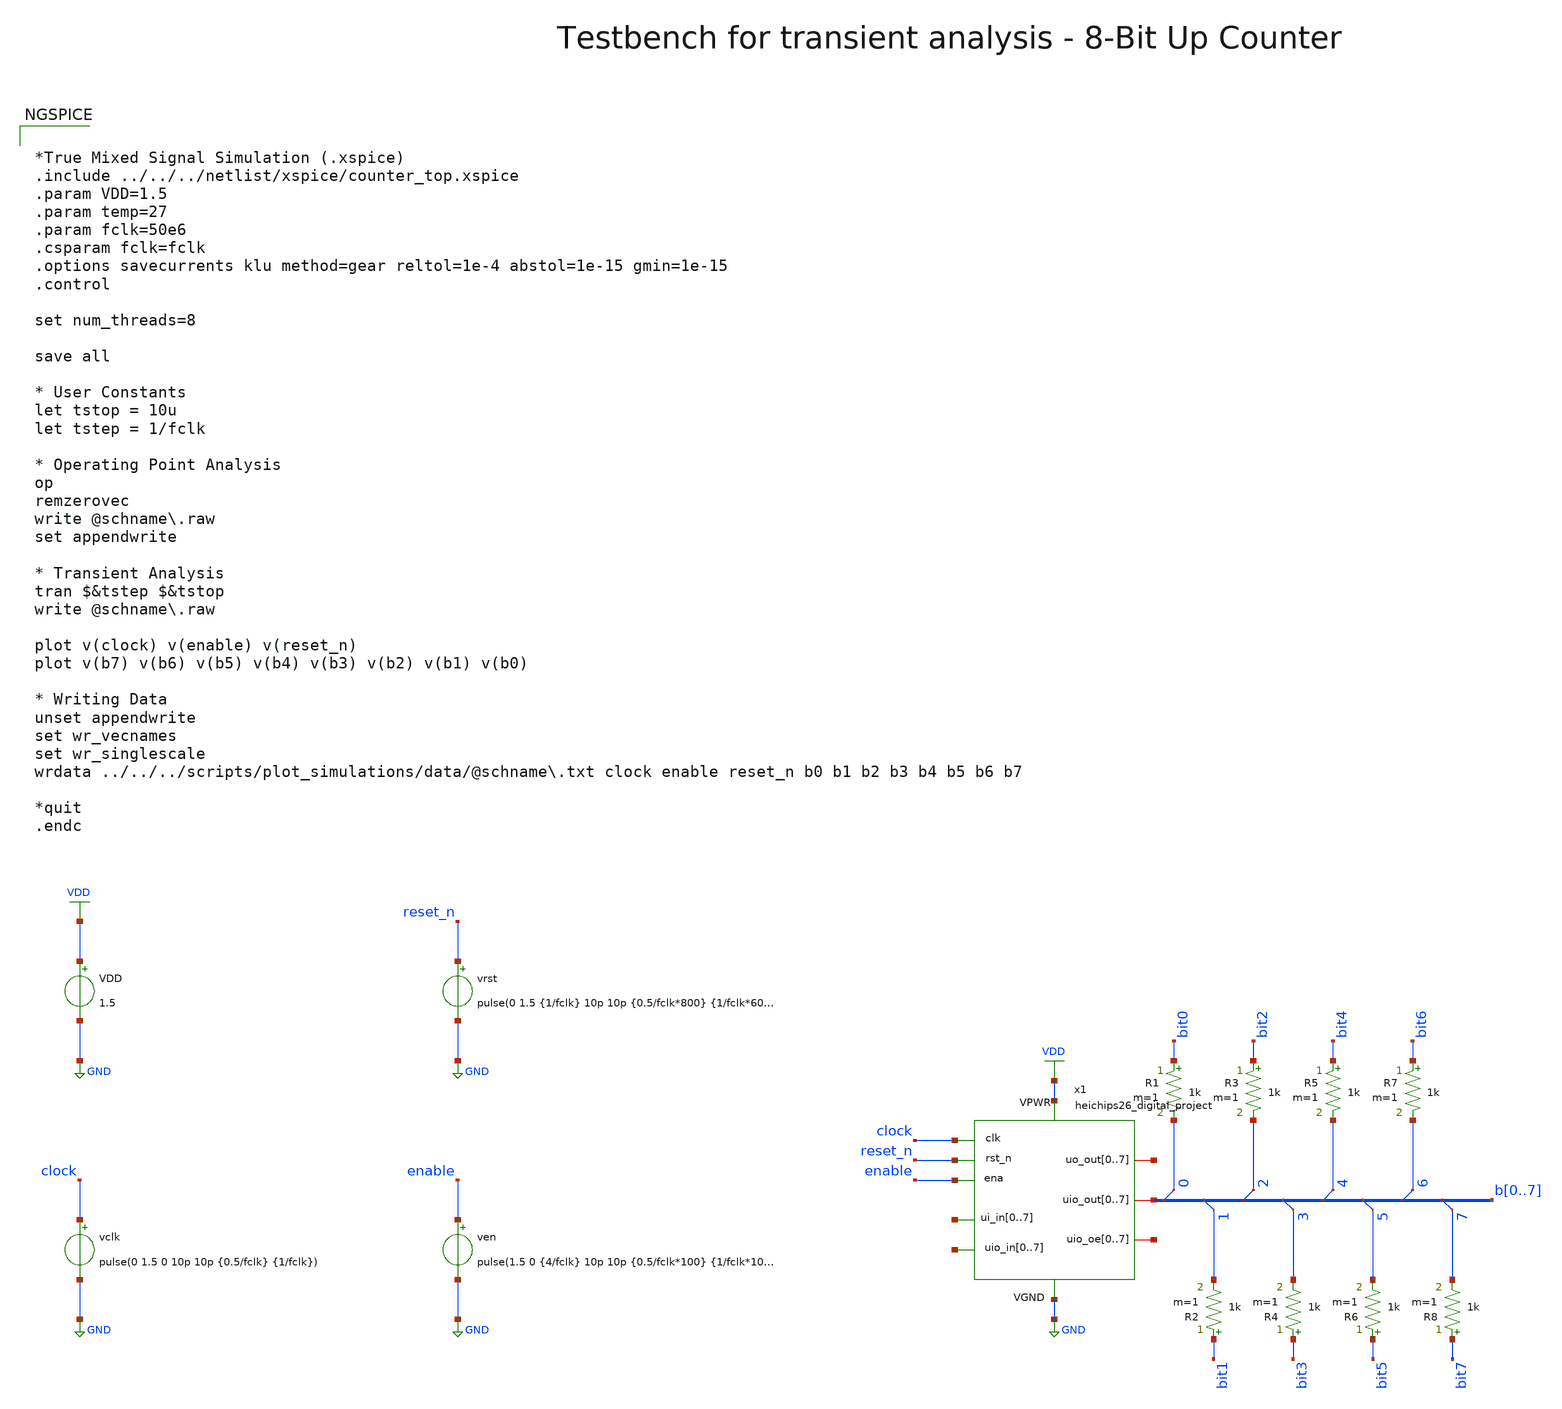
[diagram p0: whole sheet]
** sch_path: macros/heichips26_dna_sequencer/testbenches/xschem/heichips26_digital_project_tb_tran.sch
**.subckt heichips26_digital_project_tb_tran
VDD VDD GND 1.5
vclk clock GND pulse(0 1.5 0 10p 10p {0.5/fclk} {1/fclk})
vrst reset_n GND pulse(0 1.5 {1/fclk} 10p 10p {0.5/fclk*800} {1/fclk*600} 1)
ven enable GND pulse(1.5 0 {4/fclk} 10p 10p {0.5/fclk*100} {1/fclk*100} 1)
x1 VDD GND clock reset_n enable net1[7] net1[6] net1[5] net1[4] net1[3] net1[2] net1[1] net1[0]
+ net2[7] net2[6] net2[5] net2[4] net2[3] net2[2] net2[1] net2[0] net3[7] net3[6] net3[5] net3[4] net3[3]
+ net3[2] net3[1] net3[0] b0 b1 b2 b3 b4 b5 b6 b7 net4[7] net4[6] net4[5] net4[4] net4[3] net4[2] net4[1]
+ net4[0] heichips26_digital_project
* tap: b[0..7] --> b0
R1 bit0 b0 1k m=1
* tap: b[0..7] --> b1
R2 bit1 b1 1k m=1
* tap: b[0..7] --> b2
R3 bit2 b2 1k m=1
* tap: b[0..7] --> b3
R4 bit3 b3 1k m=1
* tap: b[0..7] --> b4
R5 bit4 b4 1k m=1
* tap: b[0..7] --> b5
R6 bit5 b5 1k m=1
* tap: b[0..7] --> b6
R7 bit6 b6 1k m=1
* tap: b[0..7] --> b7
R8 bit7 b7 1k m=1
**** begin user architecture code


*True Mixed Signal Simulation (.xspice)
.include ../../../netlist/xspice/counter_top.xspice
.param VDD=1.5
.param temp=27
.param fclk=50e6
.csparam fclk=fclk
.options savecurrents klu method=gear reltol=1e-4 abstol=1e-15 gmin=1e-15
.control

set num_threads=8

save all

* User Constants
let tstop = 10u
let tstep = 1/fclk

* Operating Point Analysis
op
remzerovec
write @schname\.raw
set appendwrite

* Transient Analysis
tran $&tstep $&tstop
write @schname\.raw

plot v(clock) v(enable) v(reset_n)
plot v(b7) v(b6) v(b5) v(b4) v(b3) v(b2) v(b1) v(b0)

* Writing Data
unset appendwrite
set wr_vecnames
set wr_singlescale
wrdata ../../../scripts/plot_simulations/data/@schname\.txt clock enable reset_n b0 b1 b2 b3 b4 b5
+ b6 b7

*quit
.endc


.lib cornerMOSlv.lib mos_tt
.lib cornerMOShv.lib mos_tt
.lib cornerHBT.lib hbt_typ
.lib cornerRES.lib res_typ
.lib cornerCAP.lib cap_typ
.lib cornerDIO.lib dio_tt

**** end user architecture code
**.ends
.GLOBAL GND
.GLOBAL VDD
.end
